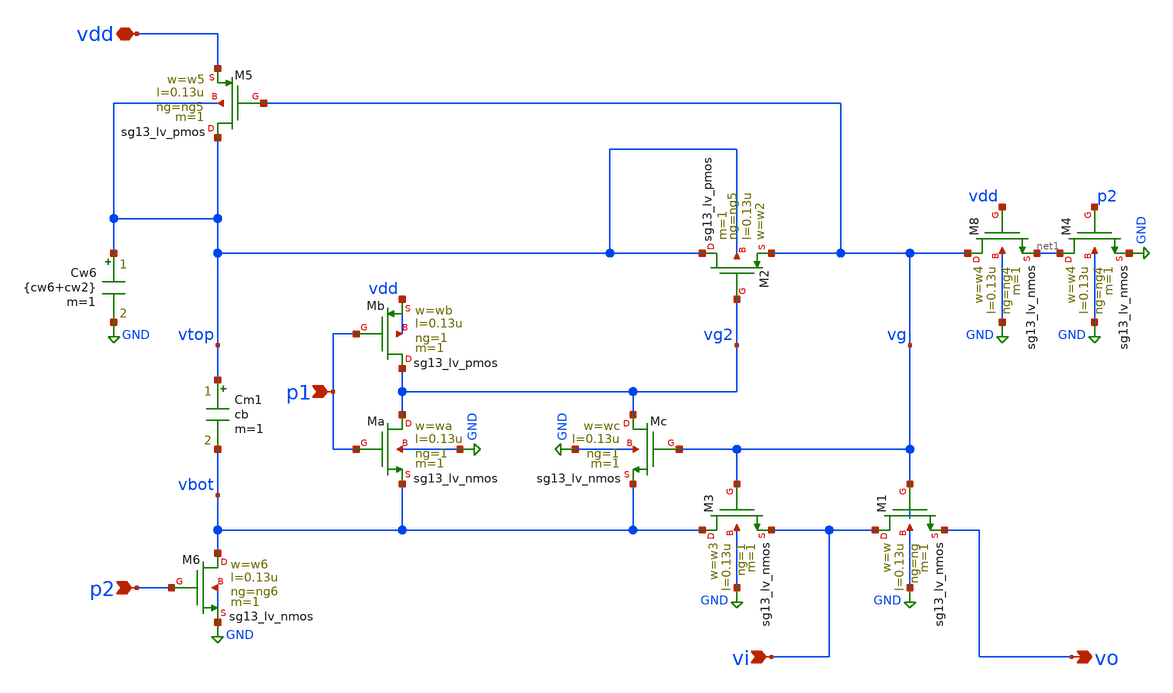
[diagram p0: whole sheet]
** sch_path: xschem/boot4.sch
**.subckt boot4 vi vo p2 vdd p1
*.ipin vi
*.opin vo
*.ipin p2
*.iopin vdd
*.ipin p1
Cm1 vtop vbot cb m=1
XM1 vi vg vo GND sg13_lv_nmos w=w l=0.13u ng=ng m=1 mm_ok=1
XM8 vg vdd net1 GND sg13_lv_nmos w=w4 l=0.13u ng=ng4 m=1 mm_ok=1
XM4 net1 p2 GND GND sg13_lv_nmos w=w4 l=0.13u ng=ng4 m=1 mm_ok=1
XM6 vbot p2 GND GND sg13_lv_nmos w=w6 l=0.13u ng=ng6 m=1 mm_ok=1
XM5 vtop vg vdd vtop sg13_lv_pmos w=w5 l=0.13u ng=ng5 m=1 mm_ok=1
Cw6 vtop GND {cw6+cw2} m=1
XM3 vbot vg vi GND sg13_lv_nmos w=w3 l=0.13u ng=1 m=1 mm_ok=1
XM2 vtop vg2 vg vtop sg13_lv_pmos w=w2 l=0.13u ng=ng5 m=1 mm_ok=1
XMb vg2 p1 vdd vdd sg13_lv_pmos w=wb l=0.13u ng=1 m=1 mm_ok=1
XMa vg2 p1 vbot GND sg13_lv_nmos w=wa l=0.13u ng=1 m=1 mm_ok=1
XMc vg2 vg vbot GND sg13_lv_nmos w=wc l=0.13u ng=1 m=1 mm_ok=1
**.ends
.GLOBAL GND
.end
